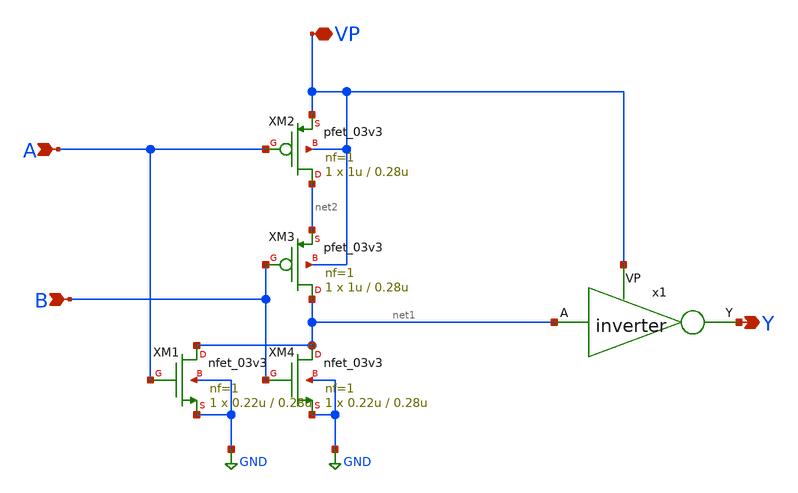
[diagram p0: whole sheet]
** sch_path: xschem/OR2.sch
**.subckt OR2 A B Y VP
*.ipin A
*.ipin B
*.opin Y
*.iopin VP
XM2 net2 A VP VP pfet_03v3 L=0.28u W=1u nf=1 ad='int((nf+1)/2) * W/nf * 0.18u' as='int((nf+2)/2) * W/nf * 0.18u'
+ pd='2*int((nf+1)/2) * (W/nf + 0.18u)' ps='2*int((nf+2)/2) * (W/nf + 0.18u)' nrd='0.18u / W' nrs='0.18u / W'
+ sa=0 sb=0 sd=0 m=1
XM4 net1 B GND GND nfet_03v3 L=0.28u W=0.22u nf=1 ad='int((nf+1)/2) * W/nf * 0.18u' as='int((nf+2)/2) * W/nf * 0.18u'
+ pd='2*int((nf+1)/2) * (W/nf + 0.18u)' ps='2*int((nf+2)/2) * (W/nf + 0.18u)' nrd='0.18u / W' nrs='0.18u / W'
+ sa=0 sb=0 sd=0 m=1
x1 VP Y net1 inverter
XM3 net1 B net2 VP pfet_03v3 L=0.28u W=1u nf=1 ad='int((nf+1)/2) * W/nf * 0.18u' as='int((nf+2)/2) * W/nf * 0.18u'
+ pd='2*int((nf+1)/2) * (W/nf + 0.18u)' ps='2*int((nf+2)/2) * (W/nf + 0.18u)' nrd='0.18u / W' nrs='0.18u / W'
+ sa=0 sb=0 sd=0 m=1
XM1 net1 A GND GND nfet_03v3 L=0.28u W=0.22u nf=1 ad='int((nf+1)/2) * W/nf * 0.18u' as='int((nf+2)/2) * W/nf * 0.18u'
+ pd='2*int((nf+1)/2) * (W/nf + 0.18u)' ps='2*int((nf+2)/2) * (W/nf + 0.18u)' nrd='0.18u / W' nrs='0.18u / W'
+ sa=0 sb=0 sd=0 m=1
**.ends

* expanding   symbol:  inverter.sym # of pins=3
** sym_path: xschem/inverter.sym
** sch_path: xschem/inverter.sch
.subckt inverter VP Y A
*.ipin A
*.opin Y
*.iopin VP
XM4 Y A GND GND nfet_03v3 L=0.28u W=0.22u nf=1 ad='int((nf+1)/2) * W/nf * 0.18u' as='int((nf+2)/2) * W/nf * 0.18u'
+ pd='2*int((nf+1)/2) * (W/nf + 0.18u)' ps='2*int((nf+2)/2) * (W/nf + 0.18u)' nrd='0.18u / W' nrs='0.18u / W'
+ sa=0 sb=0 sd=0 m=1
XM1 Y A VP VP pfet_03v3 L=0.28u W=1u nf=1 ad='int((nf+1)/2) * W/nf * 0.18u' as='int((nf+2)/2) * W/nf * 0.18u'
+ pd='2*int((nf+1)/2) * (W/nf + 0.18u)' ps='2*int((nf+2)/2) * (W/nf + 0.18u)' nrd='0.18u / W' nrs='0.18u / W'
+ sa=0 sb=0 sd=0 m=1
.ends

.GLOBAL GND
.end
